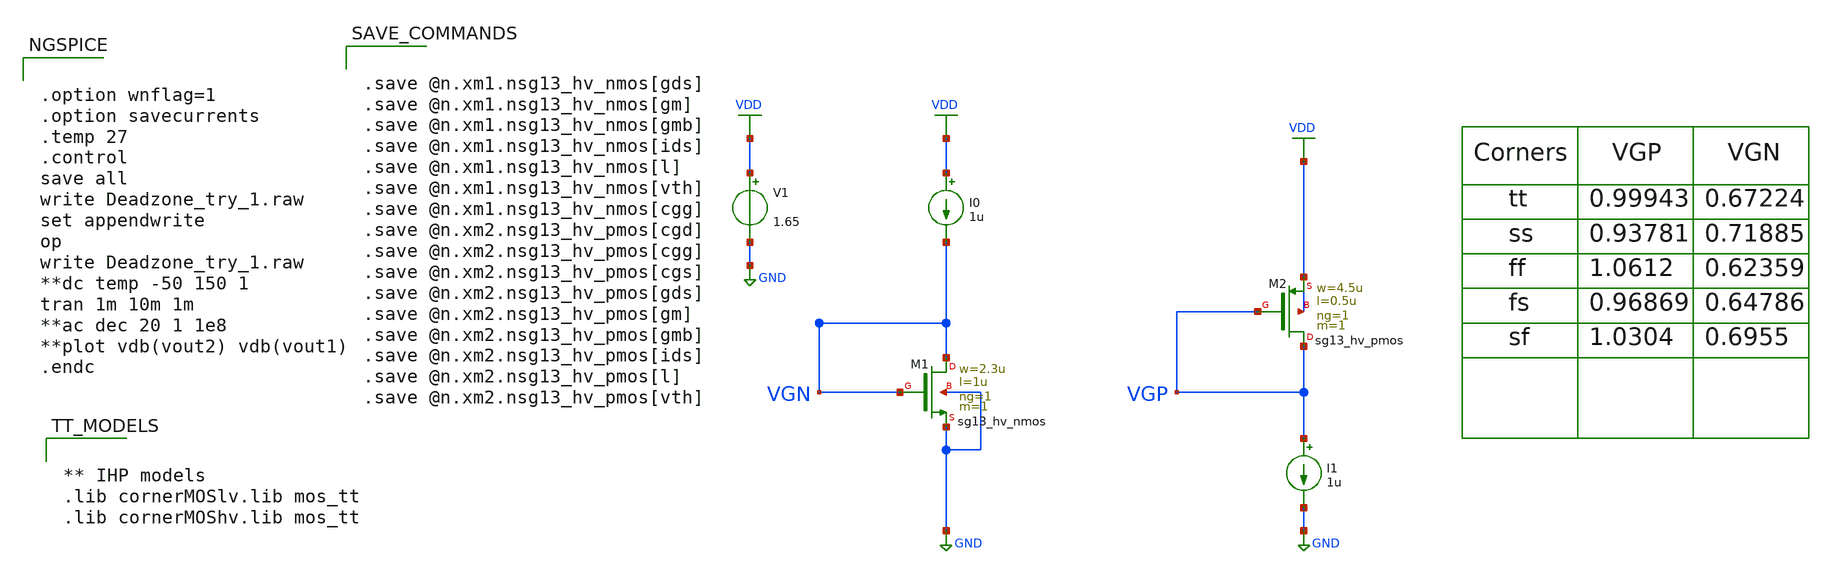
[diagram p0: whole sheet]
** sch_path: Design Files/RAMP/STG3/Deadzone_try_1.sch
**.subckt Deadzone_try_1
XM1 VGN VGN GND GND sg13_hv_nmos w=2.3u l=1u ng=1 m=1 mm_ok=1
XM2 VGP VGP VDD VDD sg13_hv_pmos w=4.5u l=0.5u ng=1 m=1 mm_ok=1
I0 VDD VGN 1u
I1 VGP GND 1u
V1 VDD GND 1.65
**** begin user architecture code


.save @n.xm1.nsg13_hv_nmos[gds]
.save @n.xm1.nsg13_hv_nmos[gm]
.save @n.xm1.nsg13_hv_nmos[gmb]
.save @n.xm1.nsg13_hv_nmos[ids]
.save @n.xm1.nsg13_hv_nmos[l]
.save @n.xm1.nsg13_hv_nmos[vth]
.save @n.xm1.nsg13_hv_nmos[cgg]
.save @n.xm2.nsg13_hv_pmos[cgd]
.save @n.xm2.nsg13_hv_pmos[cgg]
.save @n.xm2.nsg13_hv_pmos[cgs]
.save @n.xm2.nsg13_hv_pmos[gds]
.save @n.xm2.nsg13_hv_pmos[gm]
.save @n.xm2.nsg13_hv_pmos[gmb]
.save @n.xm2.nsg13_hv_pmos[ids]
.save @n.xm2.nsg13_hv_pmos[l]
.save @n.xm2.nsg13_hv_pmos[vth]




.option wnflag=1
.option savecurrents
.temp 27
.control
save all
write Deadzone_try_1.raw
set appendwrite
op
write Deadzone_try_1.raw
**dc temp -50 150 1
tran 1m 10m 1m
**ac dec 20 1 1e8
**plot vdb(vout2) vdb(vout1)
.endc




** IHP models
.lib cornerMOSlv.lib mos_tt
.lib cornerMOShv.lib mos_tt


**** end user architecture code
**.ends
.GLOBAL VDD
.GLOBAL GND
.end
